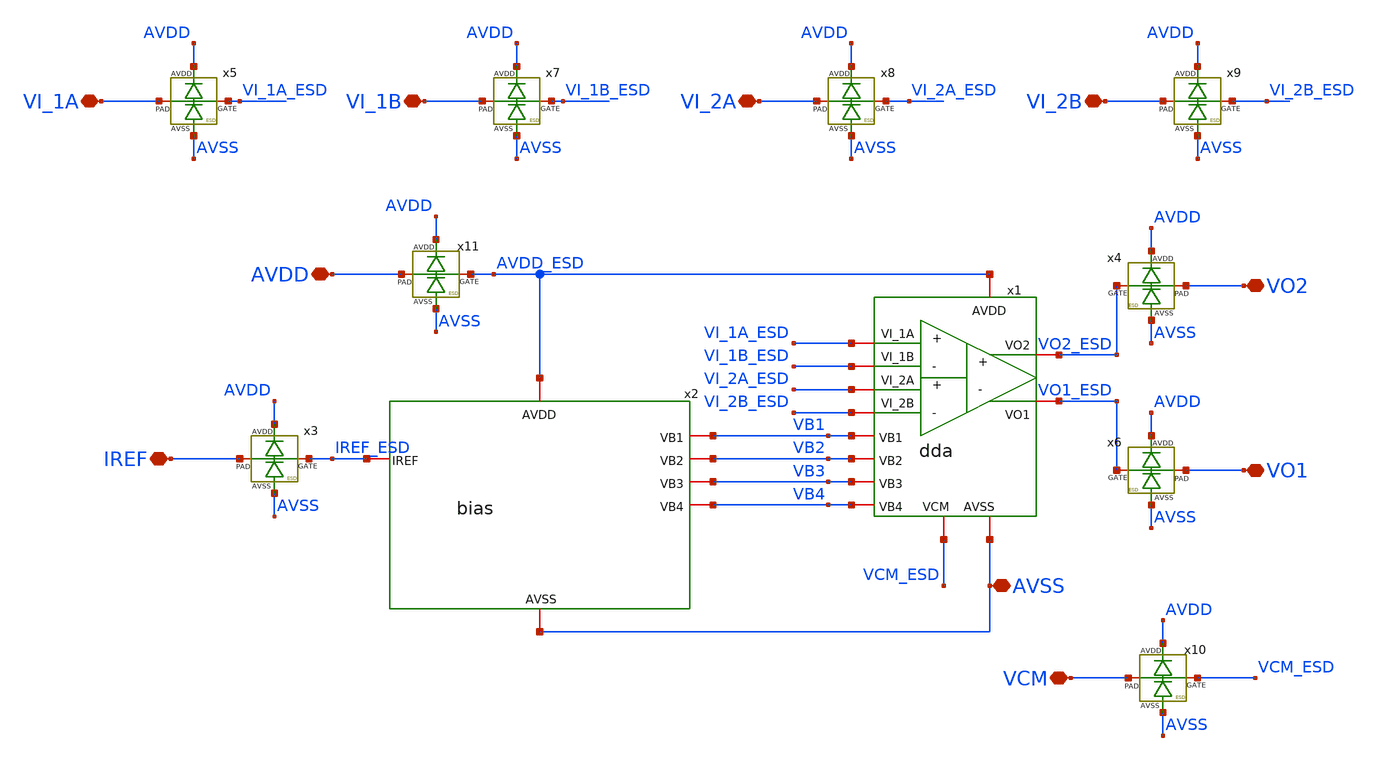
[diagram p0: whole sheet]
** sch_path: xschem/INA_layout_v2/ina_top.sch
**.subckt ina_top IREF VI_1A VI_1B VI_2A VI_2B VO2 VO1 VCM AVDD AVSS
*.iopin IREF
*.iopin VI_1A
*.iopin VI_1B
*.iopin VI_2A
*.iopin VI_2B
*.iopin VO2
*.iopin VO1
*.iopin VCM
*.iopin AVDD
*.iopin AVSS
x1 AVDD_ESD AVSS VI_1A_ESD VI_1B_ESD VO2_ESD VO1_ESD VCM_ESD VB1 VB2 VB3 VB4 VI_2A_ESD VI_2B_ESD dda
x2 IREF_ESD VB1 AVDD_ESD AVSS VB2 VB3 VB4 bias
x3 AVDD AVSS IREF IREF_ESD ESD
x4 AVDD AVSS VO2 VO2_ESD ESD
x5 AVDD AVSS VI_1A VI_1A_ESD ESD
x6 AVDD AVSS VO1 VO1_ESD ESD
x7 AVDD AVSS VI_1B VI_1B_ESD ESD
x8 AVDD AVSS VI_2A VI_2A_ESD ESD
x9 AVDD AVSS VI_2B VI_2B_ESD ESD
x10 AVDD AVSS VCM VCM_ESD ESD
x11 AVDD AVSS AVDD AVDD_ESD ESD
**.ends
.end
